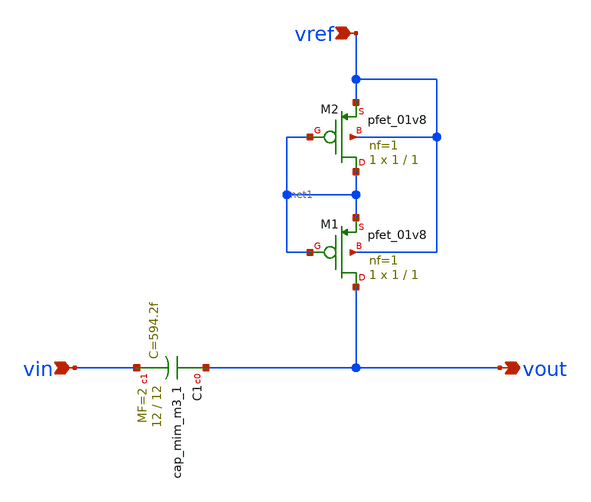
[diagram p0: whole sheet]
** sch_path: Schematic/HPF.sch
**.subckt HPF vin vout vref
*.ipin vin
*.opin vout
*.ipin vref
XC1 vout vin sky130_fd_pr__cap_mim_m3_1 W=12 L=12 MF=2 m=2
XM1 vout net1 net1 vref sky130_fd_pr__pfet_01v8 L=1 W=1 nf=1 ad='int((nf+1)/2) * W/nf * 0.29' as='int((nf+2)/2) * W/nf * 0.29'
+ pd='2*int((nf+1)/2) * (W/nf + 0.29)' ps='2*int((nf+2)/2) * (W/nf + 0.29)' nrd='0.29 / W' nrs='0.29 / W'
+ sa=0 sb=0 sd=0 mult=1 m=1
XM2 net1 net1 vref vref sky130_fd_pr__pfet_01v8 L=1 W=1 nf=1 ad='int((nf+1)/2) * W/nf * 0.29' as='int((nf+2)/2) * W/nf * 0.29'
+ pd='2*int((nf+1)/2) * (W/nf + 0.29)' ps='2*int((nf+2)/2) * (W/nf + 0.29)' nrd='0.29 / W' nrs='0.29 / W'
+ sa=0 sb=0 sd=0 mult=1 m=1
**.ends
.end
